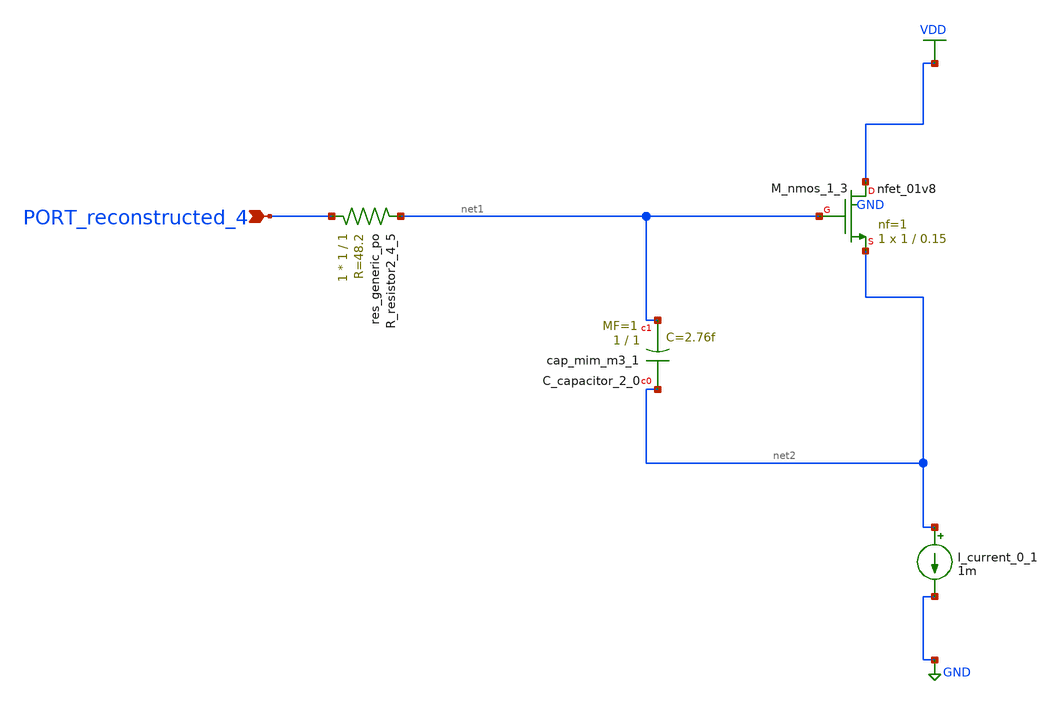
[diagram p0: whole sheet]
** sch_path: schematics/AMSNet/369.sch
**.subckt 369 PORT_reconstructed_4
*.ipin PORT_reconstructed_4
XC_capacitor_2_0 net2 net1 sky130_fd_pr__cap_mim_m3_1 W=1 L=1 MF=1 m=1
I_current_0_1 net2 GND 1m
XM_nmos_1_3 VDD net1 net2 GND sky130_fd_pr__nfet_01v8 L=0.15 W=1 nf=1 ad='int((1 + 1)/2) * 1 / 1 * 0.29'
+ as='int((1 + 2)/2) * 1 / 1 * 0.29' pd='2*int((1 + 1)/2) * (1 / 1 + 0.29)' ps='2*int((1 + 2)/2) * (1 / 1 + 0.29)'
+ nrd='0.29 / 1 ' nrs='0.29 / 1 ' sa=0 sb=0 sd=0 mult=1 m=1
XR_resistor2_4_5 PORT_reconstructed_4 net1 sky130_fd_pr__res_generic_po W=1 L=1 m=1
**.ends
.GLOBAL GND
.GLOBAL VDD
.end
